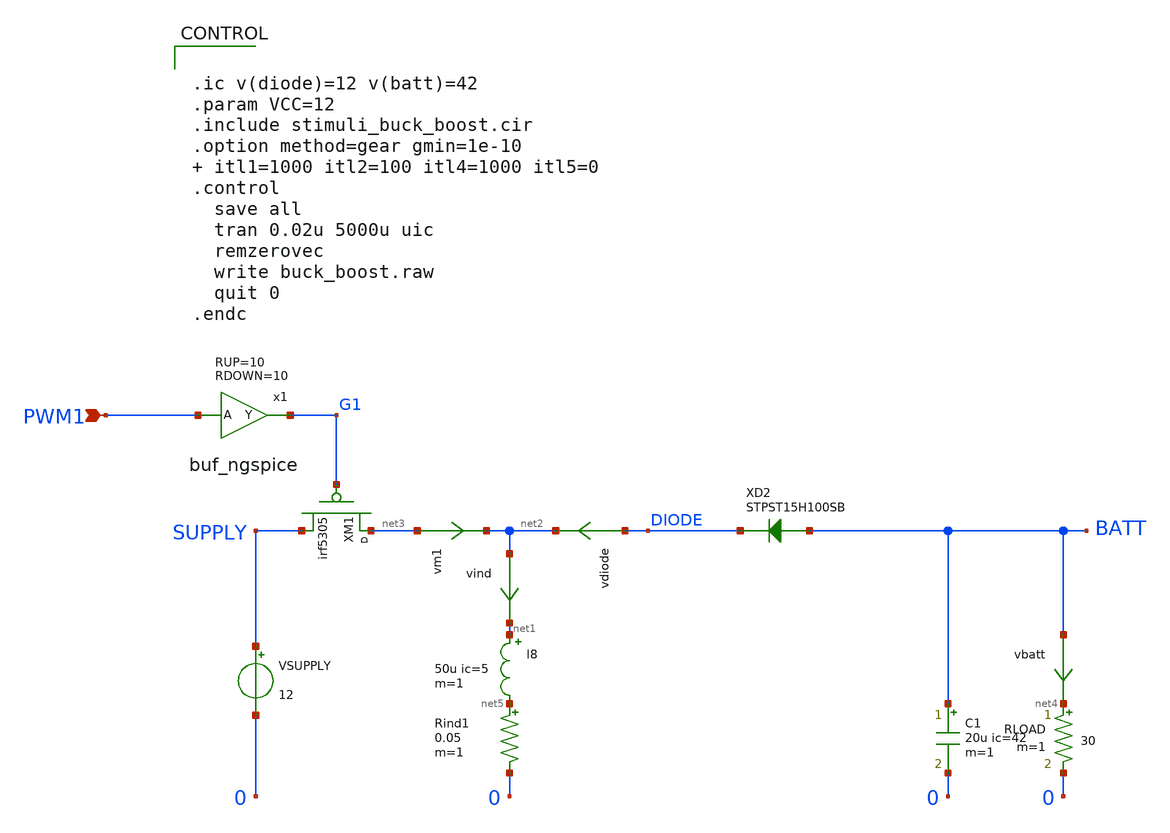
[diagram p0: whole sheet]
** sch_path: xschem_library/ngspice/buck_boost.sch
* xschem_library/ngspice/buf_ngspice.sym:
* Copyright (C) 1998-2024 Stefan Frederik Schippers
* This program is free software; you can redistribute it and/or modify
* it under the terms of the GNU General Public License as published by
* the Free Software Foundation; either version 2 of the License, or
* (at your option) any later version.
**.subckt buck_boost PWM1
*.ipin PWM1
RLOAD net4 0 30 m=1
C1 BATT 0 20u ic=42 m=1
vbatt BATT net4 0
.save i(vbatt)
vdiode DIODE net2 0
.save i(vdiode)
XD2 BATT DIODE STPST15H100SB
l8 net1 net5 50u ic=5 m=1
Rind1 net5 0 0.05 m=1
x1 G1 PWM1 buf_ngspice RUP=10 RDOWN=10
VSUPPLY SUPPLY 0 12
XM1 net3 G1 SUPPLY irf5305
vm1 net3 net2 0
.save i(vm1)
vind net2 net1 0
.save i(vind)
**.ends

* expanding   symbol:  buf_ngspice.sym # of pins=2
** sym_path: xschem_library/ngspice/buf_ngspice.sym
** sch_path: xschem_library/ngspice/buf_ngspice.sch
.subckt buf_ngspice Y A  RUP=2000 RDOWN=1000
*.ipin A
*.opin Y
B1 net1 0 V = 'VCC/2*(1+tanh((V(A1)-VCC/2)*100))'
R1 Y1 net1 ROUT m=1
C3 Y1 0 8f m=1
C1 A1 0 4f m=1
V1 Y Y1 0
V2 A1 A 0
.ends

**** begin user architecture code


.ic v(diode)=12 v(batt)=42
.param VCC=12
.include stimuli_buck_boost.cir
.option method=gear gmin=1e-10  itl1=1000 itl2=100 itl4=1000 itl5=0
.control
  save all
  tran 0.02u 5000u uic
  remzerovec
  write buck_boost.raw
  quit 0
.endc



.SUBCKT irfr5410 1 2 3
**************************************
* Model Generated by MODPEX          *
*Copyright(c) Symmetry Design Systems*
* All Rights Reserved                *
* UNPUBLISHED LICENSED SOFTWARE      *
* Contains Proprietary Information   *
* Which is The Property of           *
* SYMMETRY OR ITS LICENSORS          *
*Commercial Use or Resale Restricted *
* by Symmetry License Agreement      *
**************************************
* Model generated on Mar 8, 01
* MODEL FORMAT: SPICE3
* Symmetry POWER MOS Model (Version 1.0)
* External Node Designations
* Node 1 -> Drain
* Node 2 -> Gate
* Node 3 -> Source
M1 9 7 8 8 MM L=100u W=100u
.MODEL MM PMOS LEVEL=1 IS=1e-32 VTO=-4.10332 LAMBDA=0.044529 KP=3.57307 CGSO=5.98432e-06 CGDO=1e-11
RS 8 3 0.110361
D1 1 3 MD
.MODEL MD D IS=2.32858e-09 RS=0.0349622 N=1.5 BV=100 IBV=0.00025 EG=1 XTI=1 TT=0.0001
+ CJO=5.85483e-10 VJ=0.500001 M=0.463449 FC=0.5
RDS 3 1 1e+06
RD 9 1 0.0177033
RG 2 7 9.86001
D2 5 4 MD1
* Default values used in MD1:
* RS=0 EG=1.11 XTI=3.0 TT=0
* BV=infinite IBV=1mA
.MODEL MD1 D IS=1e-32 N=50 CJO=1.41944e-09 VJ=1.36483 M=0.723945 FC=1e-08
D3 5 0 MD2
* Default values used in MD2:
* EG=1.11 XTI=3.0 TT=0 CJO=0
* BV=infinite IBV=1mA
.MODEL MD2 D IS=1e-10 N=1 RS=3.0002e-06
RL 5 10 1
FI2 7 9 VFI2 -1
VFI2 4 0 0
EV16 10 0 9 7 1
CAP 11 10 2.27857e-09
FI1 7 9 VFI1 -1
VFI1 11 6 0
RCAP 6 10 1
D4 6 0 MD3
* Default values used in MD3:
* EG=1.11 XTI=3.0 TT=0 CJO=0
* RS=0 BV=infinite IBV=1mA
.MODEL MD3 D IS=1e-10 N=1
.ENDS irfr5410





.SUBCKT irf5305 1 2 3
**************************************
*      Model Generated by MODPEX     *
*Copyright(c) Symmetry Design Systems*
*         All Rights Reserved        *
*    UNPUBLISHED LICENSED SOFTWARE   *
*   Contains Proprietary Information *
*      Which is The Property of      *
*     SYMMETRY OR ITS LICENSORS      *
*Commercial Use or Resale Restricted *
*   by Symmetry License Agreement    *
**************************************
* Model generated on Apr 23, 96
* Model format: SPICE3
* Symmetry POWER MOS Model (Version 1.0)
* External Node Designations
* Node 1 -> Drain
* Node 2 -> Gate
* Node 3 -> Source
M1 9 7 8 8 MM L=100u W=100u
* Default values used in MM:
* The voltage-dependent capacitances are
* not included. Other default values are:
*   RS=0 RD=0 LD=0 CBD=0 CBS=0 CGBO=0
.MODEL MM PMOS LEVEL=1 IS=1e-32 VTO=-3.45761 LAMBDA=0 KP=10.066 CGSO=1.03141e-05 CGDO=1e-11
RS 8 3 0.0262305
D1 1 3 MD
.MODEL MD D IS=8.90854e-09 RS=0.00921723 N=1.5 BV=55 IBV=0.00025 EG=1.2 XTI=3.13635 TT=1e-07
+ CJO=1.30546e-09 VJ=0.663932 M=0.419045 FC=0.5
RDS 3 1 2.2e+06
RD 9 1 0.0001
RG 2 7 11.0979
D2 5 4 MD1
* Default values used in MD1:
*   RS=0 EG=1.11 XTI=3.0 TT=0
*   BV=infinite IBV=1mA
.MODEL MD1 D IS=1e-32 N=50 CJO=1.63729e-09 VJ=0.791199 M=0.552278 FC=1e-08
D3 5 0 MD2
* Default values used in MD2:
*   EG=1.11 XTI=3.0 TT=0 CJO=0
*   BV=infinite IBV=1mA
.MODEL MD2 D IS=1e-10 N=0.400245 RS=3e-06
RL 5 10 1
FI2 7 9 VFI2 -1
VFI2 4 0 0
EV16 10 0 9 7 1
CAP 11 10 1.89722e-09
FI1 7 9 VFI1 -1
VFI1 11 6 0
RCAP 6 10 1
D4 6 0 MD3
* Default values used in MD3:
*   EG=1.11 XTI=3.0 TT=0 CJO=0
*   RS=0 BV=infinite IBV=1mA
.MODEL MD3 D IS=1e-10 N=0.400245
.ENDS




*******************************************************************
* Model name       : STPST15H100SB
* Description      : 100 V - 15 A power Schottky trench diode
* Package type     : DPAK
*******************************************************************
*model STPST15H100SB  anode
*                     | cathode
*                     | |
*                     | |
.subckt STPST15H100SB 1 2
r1 1 13 0.1E-3
r2 1 13 0.1E-3
d1 13 2 dx
.model dx       D(IS=383.61E-9 N=1.0502 RS=10.043E-3 IKF=3.9178 CJO=2.0881E-9 M=1.0083  VJ=5.1229
+ ISR=262.18E-9 TT=0 EG=.69 XTI=2 FC=0.5)
.ends

**** end user architecture code
.end
